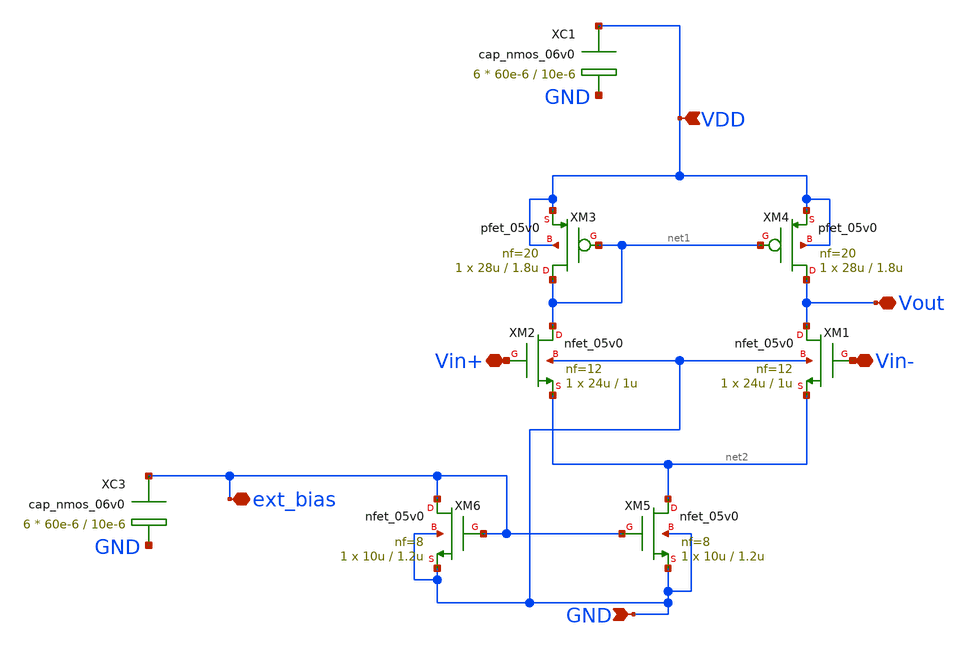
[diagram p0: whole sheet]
** sch_path: TG_gm_ff_testing/gm_ff.sch
**.subckt gm_ff GND ext_bias Vin- Vin+ Vout VDD
*.ipin GND
*.iopin ext_bias
*.iopin Vin-
*.iopin Vin+
*.iopin Vout
*.ipin VDD
XM1 Vout Vin- net2 GND nfet_05v0 L=1u W=24u nf=12 ad='int((nf+1)/2) * W/nf * 0.18u' as='int((nf+2)/2) * W/nf * 0.18u'
+ pd='2*int((nf+1)/2) * (W/nf + 0.18u)' ps='2*int((nf+2)/2) * (W/nf + 0.18u)' nrd='0.18u / W' nrs='0.18u / W'
+ sa=0 sb=0 sd=0 m=1
XM2 net1 Vin+ net2 GND nfet_05v0 L=1u W=24u nf=12 ad='int((nf+1)/2) * W/nf * 0.18u' as='int((nf+2)/2) * W/nf * 0.18u'
+ pd='2*int((nf+1)/2) * (W/nf + 0.18u)' ps='2*int((nf+2)/2) * (W/nf + 0.18u)' nrd='0.18u / W' nrs='0.18u / W'
+ sa=0 sb=0 sd=0 m=1
XM5 net2 ext_bias GND GND nfet_05v0 L=1.2u W=10u nf=8 ad='int((nf+1)/2) * W/nf * 0.18u' as='int((nf+2)/2) * W/nf * 0.18u'
+ pd='2*int((nf+1)/2) * (W/nf + 0.18u)' ps='2*int((nf+2)/2) * (W/nf + 0.18u)' nrd='0.18u / W' nrs='0.18u / W'
+ sa=0 sb=0 sd=0 m=1
XM4 Vout net1 VDD VDD pfet_05v0 L=1.8u W=28u nf=20 ad='int((nf+1)/2) * W/nf * 0.18u' as='int((nf+2)/2) * W/nf * 0.18u'
+ pd='2*int((nf+1)/2) * (W/nf + 0.18u)' ps='2*int((nf+2)/2) * (W/nf + 0.18u)' nrd='0.18u / W' nrs='0.18u / W'
+ sa=0 sb=0 sd=0 m=1
XM3 net1 net1 VDD VDD pfet_05v0 L=1.8u W=28u nf=20 ad='int((nf+1)/2) * W/nf * 0.18u' as='int((nf+2)/2) * W/nf * 0.18u'
+ pd='2*int((nf+1)/2) * (W/nf + 0.18u)' ps='2*int((nf+2)/2) * (W/nf + 0.18u)' nrd='0.18u / W' nrs='0.18u / W'
+ sa=0 sb=0 sd=0 m=1
XM6 ext_bias ext_bias GND GND nfet_05v0 L=1.2u W=10u nf=8 ad='int((nf+1)/2) * W/nf * 0.18u' as='int((nf+2)/2) * W/nf * 0.18u'
+ pd='2*int((nf+1)/2) * (W/nf + 0.18u)' ps='2*int((nf+2)/2) * (W/nf + 0.18u)' nrd='0.18u / W' nrs='0.18u / W'
+ sa=0 sb=0 sd=0 m=1
XC3 ext_bias GND cap_nmos_06v0 c_width=60e-6 c_length=10e-6 m=6
XC1 VDD GND cap_nmos_06v0 c_width=60e-6 c_length=10e-6 m=6
**.ends
.end
